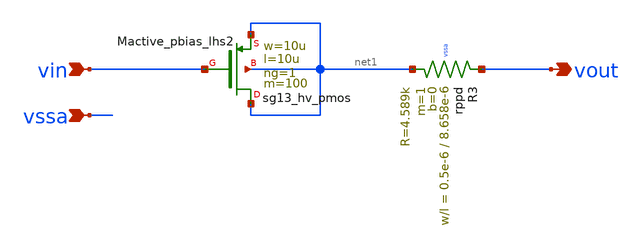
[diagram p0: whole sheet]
** sch_path: Schematics_Layout/sunrise_opamp_ncomp/sunrise_opamp_ncomp.sch
**.subckt sunrise_opamp_ncomp vout vin vssa
*.opin vout
*.ipin vin
*.ipin vssa
XMactive_pbias_lhs2 net1 vin net1 net1 sg13_hv_pmos w=10u l=10u ng=1 m=100 mm_ok=1
XR3 vout net1 vssa rppd w=0.5e-6 l=8.658e-6 m=1 b=0 mm_ok=1
**.ends
.end
